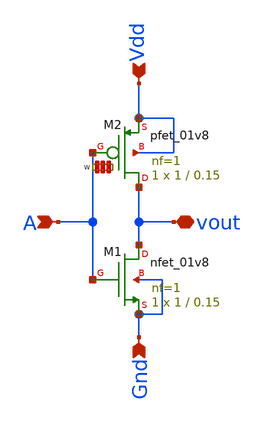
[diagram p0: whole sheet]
** sch_path: inv.sch
**.subckt inv vout A Vdd Gnd
*.iopin vout
*.ipin A
*.ipin Vdd
*.ipin Gnd
XM1 vout A Gnd Gnd sky130_fd_pr__nfet_01v8 L=0.15 W=1 nf=1 ad='int((1 + 1)/2) * 1 / 1 * 0.29' as='int((1 + 2)/2) * 1 / 1 * 0.29'
+ pd='2*int((1 + 1)/2) * (1 / 1 + 0.29)' ps='2*int((1 + 2)/2) * (1 / 1 + 0.29)' nrd='0.29 / 1 ' nrs='0.29 / 1 '
+ sa=0 sb=0 sd=0 mult=1 m=1
XM2 vout A Vdd Vdd sky130_fd_pr__pfet_01v8 L=0.15 W='1 * 1 ' nf=1 ad='int((1 + 1)/2) * 1 / 1 * 0.29'
+ as='int((1 + 2)/2) * 1 / 1 * 0.29' pd='2*int((1 + 1)/2) * (1 / 1 + 0.29)' ps='2*int((1 + 2)/2) * (1 / 1 + 0.29)'
+ nrd='0.29 / 1 ' nrs='0.29 / 1 ' sa=0 sb=0 sd=0 mult=1 m=1
**.ends
.end
